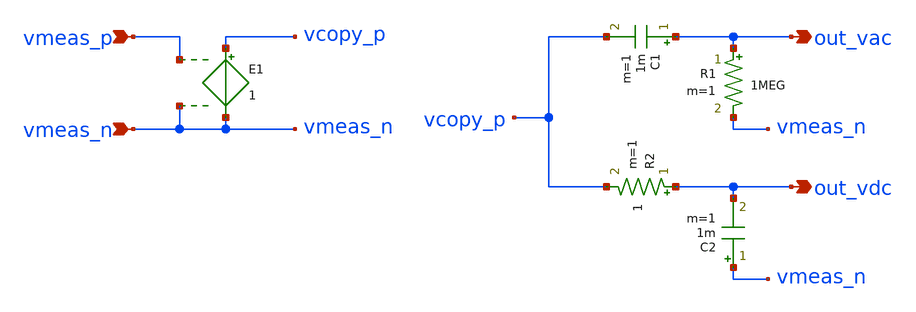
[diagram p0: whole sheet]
** sch_path: Utilities/ProbeBlock/Probe__V-AC-DC.sch
**.subckt Probe__V-AC-DC vmeas_p out_vac out_vdc vmeas_n
*.ipin vmeas_p
*.opin out_vac
*.opin out_vdc
*.ipin vmeas_n
E1 vcopy_p vmeas_n vmeas_p vmeas_n 1
C1 out_vac vcopy_p 1m m=1
R1 out_vac vmeas_n 1MEG m=1
C2 vmeas_n out_vdc 1m m=1
R2 out_vdc vcopy_p 1 m=1
**.ends
.end
